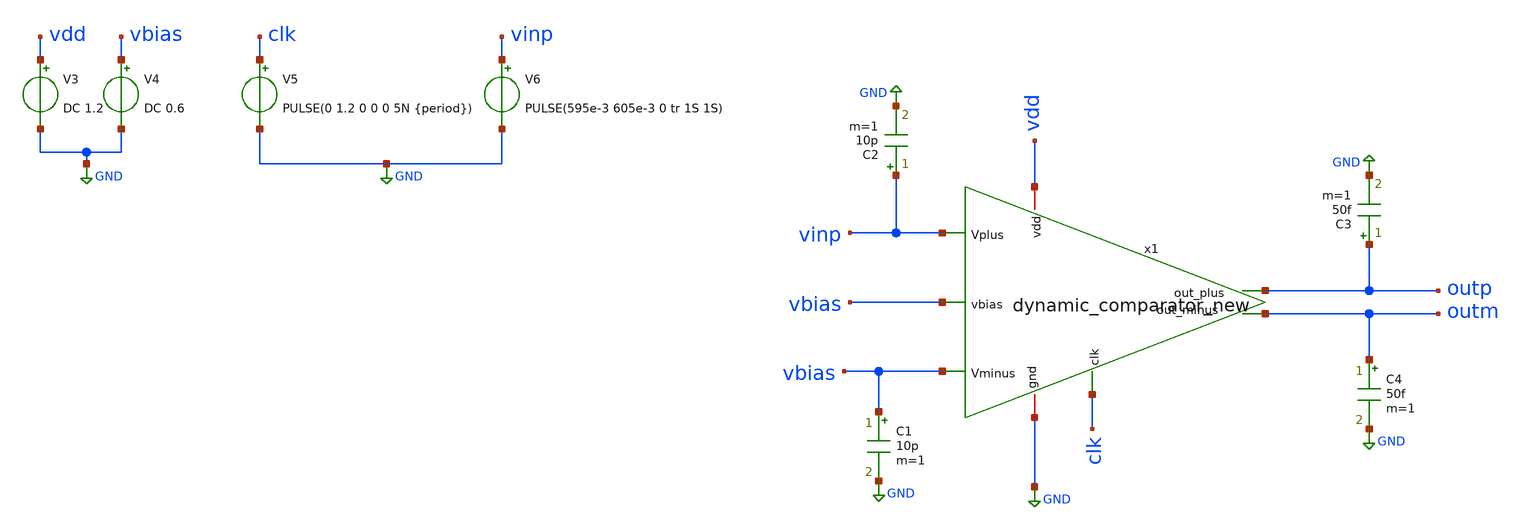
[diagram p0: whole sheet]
** sch_path: testbench/dynamicComparator_tb.sch
**.subckt dynamicComparator_tb
C1 vbias GND 10p m=1
C2 vinp GND 10p m=1
C3 outp GND 50f m=1
C4 outm GND 50f m=1
V3 vdd GND DC 1.2
V4 vbias GND DC 0.6
V5 clk GND PULSE(0 1.2 0 0 0 5N {period})
V6 vinp GND PULSE(595e-3 605e-3 0 tr 1S 1S)
x1 vdd vbias vinp vbias outm outp clk GND dynamic_comparator_new
**** begin user architecture code

.lib cornerMOSlv.lib mos_tt
.lib cornerRES.lib res_typ



.param temp=27
.param clock = 100e6       ; 100 MHz clock
.param period = {1/clock}
.param num_cycles = 100
.param tr = {num_cycles * period}
.meas TRAN i_comp AVG i(V3) FROM=100n TO=1000n
.control
save all
* Operating point simulation
op
write comparator_tb.raw
set appendwrite

* Transient analysis
.options meas_step_max=1e-10
tran 500p 1u
let vindiff = v(vinp) - v(vbias)
let clk = v(clk)
let vout = v(outp) - v(outm)
let p_comp = abs(i_comp) * 1.2
print p_comp
meas TRAN rise_time TRIG v(outp) VAL=0.12  TD=9n RISE=4 TARG v(outp) VAL=1.08 TD=9n RISE=4
meas TRAN fall_time TRIG v(outp) VAL=1.08  TD=9n RISE=4 TARG v(outp) VAL=0.12 TD=9n RISE=4

write comparator_tb.raw
.endc


**** end user architecture code
**.ends

* expanding   symbol:  dynamic_comparator_new.sym # of pins=8
** sym_path: schematic/dynamic_comparator_new.sym
** sch_path: schematic/dynamic_comparator_new.sch
.subckt dynamic_comparator_new vdd vbias Vplus Vminus out_minus out_plus clk gnd
*.ipin vbias
*.opin out_plus
*.opin out_minus
*.iopin gnd
*.iopin vdd
*.ipin Vplus
*.ipin Vminus
*.ipin clk
XM8 net4 vbias vdd well sg13_lv_pmos w=18u l=0.3u ng=4 m=1 mm_ok=1
XM20 net1 clk net4 well sg13_lv_pmos w=18u l=0.300u ng=4 m=1 mm_ok=1
XM21 net2 outp net1 well sg13_lv_pmos w=32u l=300n ng=4 m=1 mm_ok=1
XM22 net3 outn net1 well sg13_lv_pmos w=32u l=300n ng=4 m=1 mm_ok=1
XM23 gnd clk net2 sub! sg13_lv_nmos w=4.0u l=0.200u ng=1 m=1 mm_ok=1
XM24 gnd net3 net2 sub! sg13_lv_nmos w=4.0u l=0.200u ng=1 m=1 mm_ok=1
XM25 gnd clk net3 sub! sg13_lv_nmos w=4.0u l=0.200u ng=1 m=1 mm_ok=1
XM26 gnd net2 net3 sub! sg13_lv_nmos w=4.0u l=0.200u ng=1 m=1 mm_ok=1
XM27 gnd net2 out_plus sub! sg13_lv_nmos w=4.0u l=0.2u ng=1 m=1 mm_ok=1
XM28 gnd net3 out_minus sub! sg13_lv_nmos w=4.0u l=0.200u ng=1 m=1 mm_ok=1
XM29 out_minus net3 vdd well sg13_lv_pmos w=8u l=0.200u ng=1 m=1 mm_ok=1
XM30 out_plus net2 vdd well sg13_lv_pmos w=8u l=0.200u ng=1 m=1 mm_ok=1
XM32 outn Vplus net5 well sg13_lv_pmos w=8u l=0.3u ng=2 m=1 mm_ok=1
XM33 outp Vminus net5 well sg13_lv_pmos w=8u l=0.3u ng=2 m=1 mm_ok=1
XM1 net5 vbias vdd well sg13_lv_pmos w=12u l=0.8u ng=2 m=1 mm_ok=1
XR1 outn gnd sub! rppd w=2.5e-6 l=13.595e-6 m=1 b=6 mm_ok=1
XR2 outp gnd sub! rppd w=2.5e-6 l=18.02e-6 m=1 b=6 mm_ok=1
XR3 vdd well ntap1 R=262.8 w=0.78e-6 l=0.78e-6
XR4 gnd sub! ptap1 R=262.8 w=0.78e-6 l=0.78e-6
.ends

.GLOBAL GND
.end
